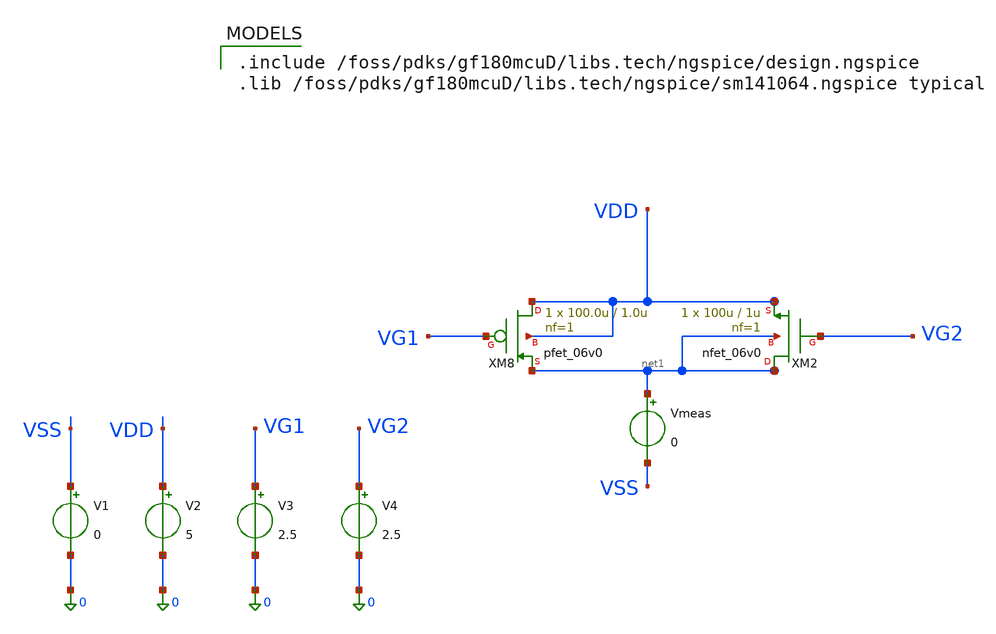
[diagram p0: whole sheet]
** sch_path: activities/opamp3AKAM/simulations_testbench/resistance.sch
**.subckt resistance
XM2 net1 VG2 VDD net1 nfet_06v0 L=1u W=100u nf=1 ad='int((nf+1)/2) * W/nf * 0.18u' as='int((nf+2)/2) * W/nf * 0.18u'
+ pd='2*int((nf+1)/2) * (W/nf + 0.18u)' ps='2*int((nf+2)/2) * (W/nf + 0.18u)' nrd='0.18u / W' nrs='0.18u / W'
+ sa=0 sb=0 sd=0 m=1
XM8 VDD VG1 net1 VDD pfet_06v0 L=1.0u W=100.0u nf=1 ad='int((nf+1)/2) * W/nf * 0.18u' as='int((nf+2)/2) * W/nf * 0.18u'
+ pd='2*int((nf+1)/2) * (W/nf + 0.18u)' ps='2*int((nf+2)/2) * (W/nf + 0.18u)' nrd='0.18u / W' nrs='0.18u / W'
+ sa=0 sb=0 sd=0 m=1
V1 VSS 0 0
V2 VDD 0 5
V3 VG1 0 2.5
V4 VG2 0 2.5
Vmeas net1 VSS 0
**** begin user architecture code

.include /foss/pdks/gf180mcuD/libs.tech/ngspice/design.ngspice
.lib /foss/pdks/gf180mcuD/libs.tech/ngspice/sm141064.ngspice typical



.control
op
echo "VG1 VG2 Resistance" >
+ /foss/designs/sscs-2026-zotnetic/activities/opamp3AKAM/simulations_results/resistance.txt
let b1 = 0
let b2 = 0

while b1 <= 5
    alter v3 $&b1
    while b2 <=5
	alter v4 $&b2
	let b3 = v(VDD)/i(Vmeas)
	echo "$&b1 $&b2 $&b3" >>
+ /foss/designs/sscs-2026-zotnetic/activities/opamp3AKAM/simulations_results/resistance.txt
	let b2 = b2 +0.5
    end
    let b2 = 0
    let b1 = b1 +0.5
end

.endc

**** end user architecture code
**.ends
.end
